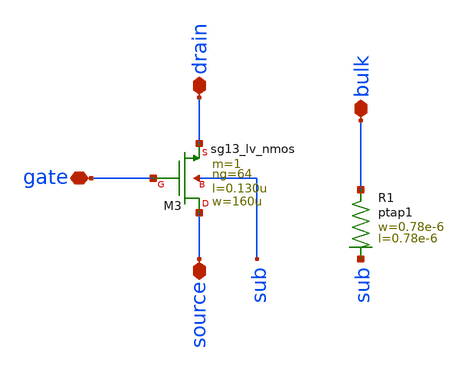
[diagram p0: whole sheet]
** sch_path: ts_pr_May2024/design_data/xschem/nmos64.sch
**.subckt nmos64 drain source bulk gate
*.iopin drain
*.iopin source
*.iopin bulk
*.iopin gate
XR1 bulk sub ptap1 R=262.8 w=0.78e-6 l=0.78e-6
XM3 source gate drain sub sg13_lv_nmos w=160u l=0.130u ng=64 m=1 mm_ok=1
**.ends
.end
